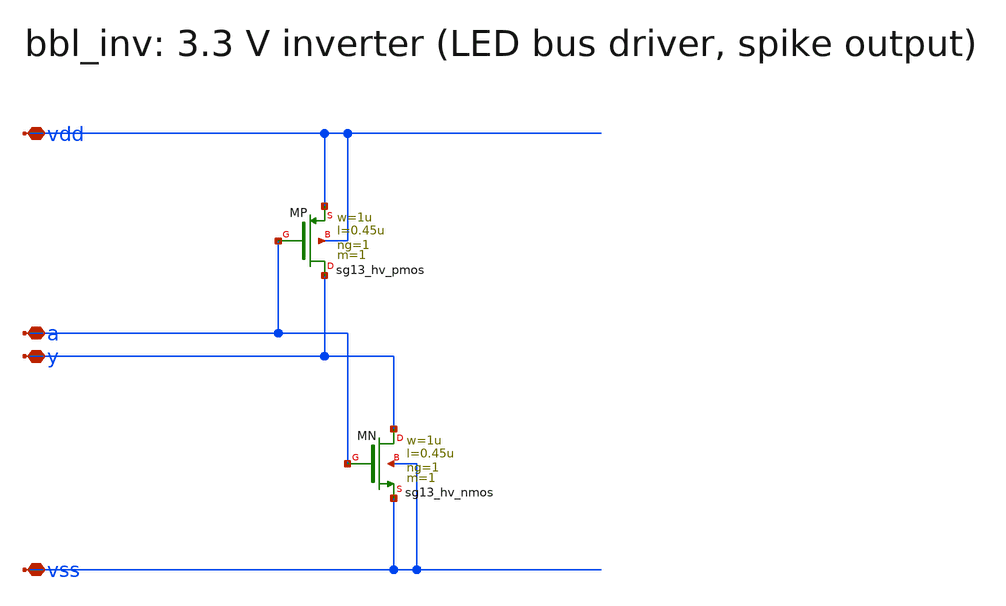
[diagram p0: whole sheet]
** sch_path: schematic/xschem/bbl_inv.sch
**.subckt bbl_inv vdd vss a y
*.iopin vdd
*.iopin vss
*.iopin a
*.iopin y
XMP y a vdd vdd sg13_hv_pmos w=1u l=0.45u ng=1 m=1 mm_ok=1
XMN y a vss vss sg13_hv_nmos w=1u l=0.45u ng=1 m=1 mm_ok=1
**.ends
.end
